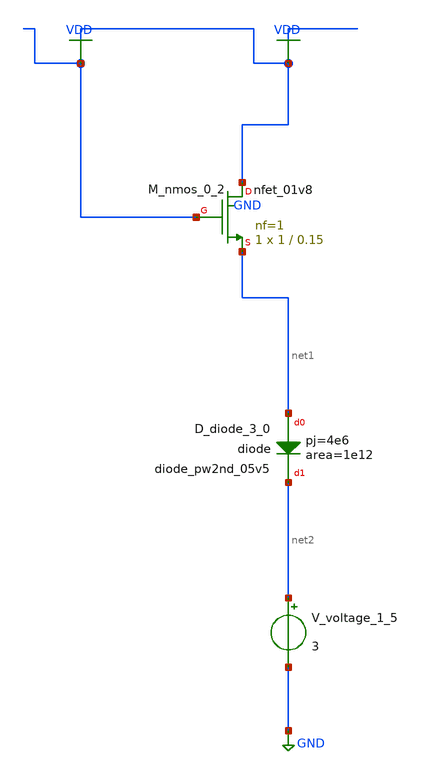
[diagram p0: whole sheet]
** sch_path: schematics/AMSNet/24.sch
**.subckt 24
XD_diode_3_0 net1 net2 sky130_fd_pr__diode_pw2nd_05v5 area=1e12 pj=4e6
XM_nmos_0_2 VDD VDD net1 GND sky130_fd_pr__nfet_01v8 L=0.15 W=1 nf=1 ad='int((1 + 1)/2) * 1 / 1 * 0.29'
+ as='int((1 + 2)/2) * 1 / 1 * 0.29' pd='2*int((1 + 1)/2) * (1 / 1 + 0.29)' ps='2*int((1 + 2)/2) * (1 / 1 + 0.29)'
+ nrd='0.29 / 1 ' nrs='0.29 / 1 ' sa=0 sb=0 sd=0 mult=1 m=1
V_voltage_1_5 net2 GND 3
**.ends
.GLOBAL GND
.GLOBAL VDD
.end
